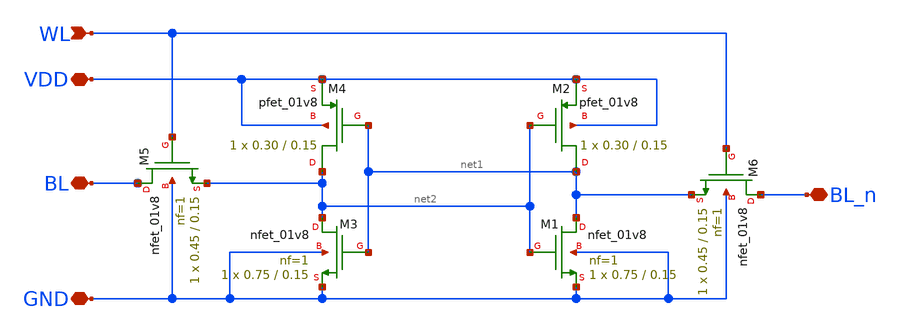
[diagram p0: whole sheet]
** sch_path: SRAM_cell.sch
**.subckt SRAM_cell BL BL_n WL VDD GND
*.iopin BL
*.iopin BL_n
*.ipin WL
*.iopin VDD
*.iopin GND
XM2 net1 net2 VDD VDD sky130_fd_pr__pfet_01v8 W=0.30 L=0.15 ad='int((nf+1)/2) * W/nf * 0.29' pd='2*int((nf+1)/2) * (W/nf + 0.29)'
+ as='int((nf+2)/2) * W/nf * 0.29' ps='2*int((nf+2)/2) * (W/nf + 0.29)' nrd='0.29 / W' nrs='0.29 / W' sa=0
+ sb=0 sd=0 nf=1 mult=1
XM4 net2 net1 VDD VDD sky130_fd_pr__pfet_01v8 W=0.30 L=0.15 ad='int((nf+1)/2) * W/nf * 0.29' pd='2*int((nf+1)/2) * (W/nf + 0.29)'
+ as='int((nf+2)/2) * W/nf * 0.29' ps='2*int((nf+2)/2) * (W/nf + 0.29)' nrd='0.29 / W' nrs='0.29 / W' sa=0
+ sb=0 sd=0 nf=1 mult=1
XM5 BL WL net2 GND sky130_fd_pr__nfet_01v8 L=0.15 W=0.45 nf=1 ad='int((nf+1)/2) * W/nf * 0.29' as='int((nf+2)/2) * W/nf * 0.29'
+ pd='2*int((nf+1)/2) * (W/nf + 0.29)' ps='2*int((nf+2)/2) * (W/nf + 0.29)' nrd='0.29 / W' nrs='0.29 / W'
+ sa=0 sb=0 sd=0 mult=1 m=1
XM6 BL_n WL net1 GND sky130_fd_pr__nfet_01v8 L=0.15 W=0.45 nf=1 ad='int((nf+1)/2) * W/nf * 0.29' as='int((nf+2)/2) * W/nf * 0.29'
+ pd='2*int((nf+1)/2) * (W/nf + 0.29)' ps='2*int((nf+2)/2) * (W/nf + 0.29)' nrd='0.29 / W' nrs='0.29 / W'
+ sa=0 sb=0 sd=0 mult=1 m=1
XM1 net1 net2 GND GND sky130_fd_pr__nfet_01v8 L=0.15 W=0.75 nf=1 ad='int((nf+1)/2) * W/nf * 0.29' as='int((nf+2)/2) * W/nf * 0.29'
+ pd='2*int((nf+1)/2) * (W/nf + 0.29)' ps='2*int((nf+2)/2) * (W/nf + 0.29)' nrd='0.29 / W' nrs='0.29 / W'
+ sa=0 sb=0 sd=0 mult=1 m=1
XM3 net2 net1 GND GND sky130_fd_pr__nfet_01v8 L=0.15 W=0.75 nf=1 ad='int((nf+1)/2) * W/nf * 0.29' as='int((nf+2)/2) * W/nf * 0.29'
+ pd='2*int((nf+1)/2) * (W/nf + 0.29)' ps='2*int((nf+2)/2) * (W/nf + 0.29)' nrd='0.29 / W' nrs='0.29 / W'
+ sa=0 sb=0 sd=0 mult=1 m=1
**.ends
.end
